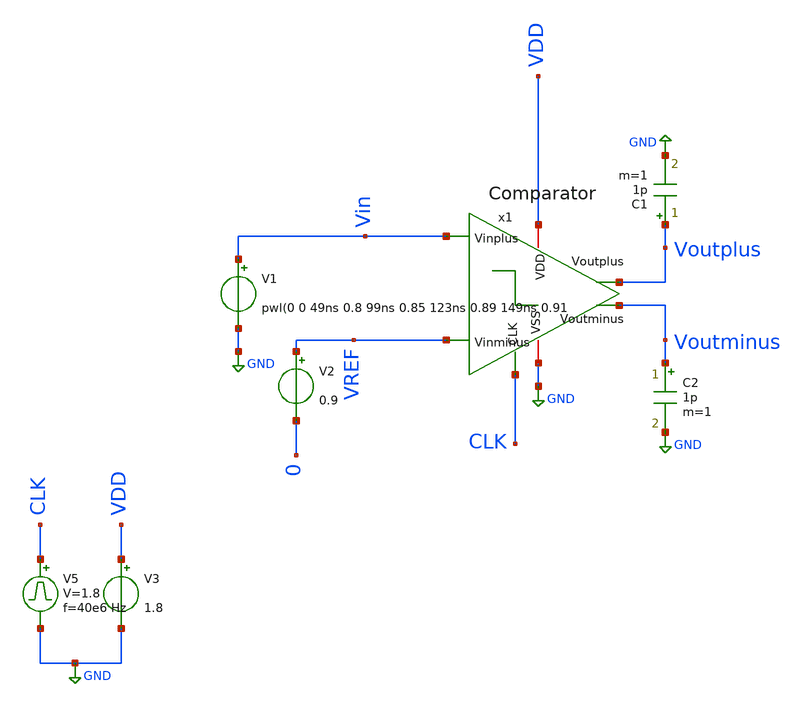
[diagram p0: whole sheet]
** sch_path: xschem/TestBenches/ComparatorTb_MC.sch
**.subckt ComparatorTb_MC
V2 VREF 0 0.9
V3 VDD GND 1.8
.save i(v3)
V1 Vin GND pwl(0 0 49ns 0.8 99ns 0.85 123ns 0.89 149ns 0.91
C1 Voutplus GND 1p m=1
C2 Voutminus GND 1p m=1
V5 CLK GND pulse 0 1.8 '0.495/ 40e6 ' '0.01/40e6 ' '0.01/40e6 ' '0.49/40e6 ' '1/40e6 '
x1 VDD Voutminus Voutplus CLK Vin VREF GND Comparator
**** begin user architecture code


.savecurrents
.control
 save all
  set wr_vecnames
  set wr_singlescale

  let mc_runs = 10
  let run = 1
  dowhile run <= mc_runs
   tran 1e-9 200e-9
   wrdata ADC4bitMC{$&run}.txt Vin x2.out0 x2.out1 x2.out2 x2.out3
   reset
   let run = run + 1
  end
end
.endc


 .option wnflag=1
** opencircuitdesign pdks install
.param MC_SWITCH=1.0
.lib $::SKYWATER_MODELS/sky130.lib.spice mm


**** end user architecture code
**.ends
.GLOBAL GND
.end
